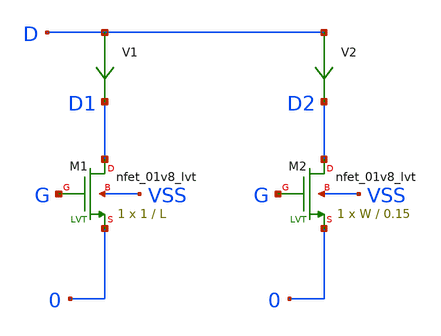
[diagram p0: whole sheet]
** sch_path: xyce/sky130A-xyce/libs.tech/xschem/sky130_tests/test_nmos_sizes.sch
* Copyright 2020 Stefan Frederik Schippers
* Licensed under the Apache License, Version 2.0 (the "License");
* you may not use this file except in compliance with the License.
* You may obtain a copy of the License at
* https://www.apache.org/licenses/LICENSE-2.0
* Unless required by applicable law or agreed to in writing, software
* distributed under the License is distributed on an "AS IS" BASIS,
* WITHOUT WARRANTIES OR CONDITIONS OF ANY KIND, either express or implied.
* See the License for the specific language governing permissions and
* limitations under the License.
**.subckt test_nmos_sizes
XM1 D1 G 0 VSS sky130_fd_pr__nfet_01v8_lvt L=L W=1 nf=1 ad='W * 0.29' as='W * 0.29' pd='2 * (W + 0.29)'
+ ps='2 * (W + 0.29)' nrd='0.29 / W' nrs='0.29 / W' sa=0 sb=0 sd=0 mult=1 m=1
XM2 D2 G 0 VSS sky130_fd_pr__nfet_01v8_lvt L=0.15 W=W nf=1 ad='W * 0.29' as='W * 0.29' pd='2 * (W + 0.29)'
+ ps='2 * (W + 0.29)' nrd='0.29 / W' nrs='0.29 / W' sa=0 sb=0 sd=0 mult=1 m=1
V2 D D2 0
.save i(v2)
V1 D D1 0
.save i(v1)
**** begin user architecture code

.include $::SKYWATER_MODELS/cells/nfet_01v8/sky130_fd_pr__nfet_01v8__tt.corner.spice
.include $::SKYWATER_MODELS/cells/nfet_01v8_lvt/sky130_fd_pr__nfet_01v8_lvt__tt.corner.spice
.include $::SKYWATER_MODELS/cells/pfet_01v8/sky130_fd_pr__pfet_01v8__tt.corner.spice
.include $::SKYWATER_MODELS/cells/nfet_03v3_nvt/sky130_fd_pr__nfet_03v3_nvt__tt.corner.spice
.include $::SKYWATER_MODELS/cells/nfet_05v0_nvt/sky130_fd_pr__nfet_05v0_nvt__tt.corner.spice
.include $::SKYWATER_MODELS/cells/esd_nfet_01v8/sky130_fd_pr__esd_nfet_01v8__tt.corner.spice
.include $::SKYWATER_MODELS/cells/pfet_01v8_lvt/sky130_fd_pr__pfet_01v8_lvt__tt.corner.spice
.include $::SKYWATER_MODELS/cells/pfet_01v8_hvt/sky130_fd_pr__pfet_01v8_hvt__tt.corner.spice
.include $::SKYWATER_MODELS/cells/esd_pfet_g5v0d10v5/sky130_fd_pr__esd_pfet_g5v0d10v5__tt.corner.spice
.include $::SKYWATER_MODELS/cells/pfet_g5v0d10v5/sky130_fd_pr__pfet_g5v0d10v5__tt.corner.spice
.include $::SKYWATER_MODELS/cells/pfet_g5v0d16v0/sky130_fd_pr__pfet_g5v0d16v0__tt.corner.spice
.include $::SKYWATER_MODELS/cells/nfet_g5v0d10v5/sky130_fd_pr__nfet_g5v0d10v5__tt.corner.spice
.include $::SKYWATER_MODELS/cells/nfet_g5v0d16v0/sky130_fd_pr__nfet_g5v0d16v0__tt_discrete.corner.spice
.include $::SKYWATER_MODELS/cells/esd_nfet_g5v0d10v5/sky130_fd_pr__esd_nfet_g5v0d10v5__tt.corner.spice
.include $::SKYWATER_MODELS/models/corners/tt/nonfet.spice
* Mismatch parameters
.include $::SKYWATER_MODELS/cells/nfet_01v8/sky130_fd_pr__nfet_01v8__mismatch.corner.spice
.include $::SKYWATER_MODELS/cells/pfet_01v8/sky130_fd_pr__pfet_01v8__mismatch.corner.spice
.include $::SKYWATER_MODELS/cells/nfet_01v8_lvt/sky130_fd_pr__nfet_01v8_lvt__mismatch.corner.spice
.include $::SKYWATER_MODELS/cells/pfet_01v8_lvt/sky130_fd_pr__pfet_01v8_lvt__mismatch.corner.spice
.include $::SKYWATER_MODELS/cells/pfet_01v8_hvt/sky130_fd_pr__pfet_01v8_hvt__mismatch.corner.spice
.include $::SKYWATER_MODELS/cells/nfet_g5v0d10v5/sky130_fd_pr__nfet_g5v0d10v5__mismatch.corner.spice
.include $::SKYWATER_MODELS/cells/pfet_g5v0d10v5/sky130_fd_pr__pfet_g5v0d10v5__mismatch.corner.spice
.include $::SKYWATER_MODELS/cells/nfet_05v0_nvt/sky130_fd_pr__nfet_05v0_nvt__mismatch.corner.spice
.include $::SKYWATER_MODELS/cells/nfet_03v3_nvt/sky130_fd_pr__nfet_03v3_nvt__mismatch.corner.spice
* Resistor$::SKYWATER_MODELS/Capacitor
.include $::SKYWATER_MODELS/models/r+c/res_typical__cap_typical.spice
.include $::SKYWATER_MODELS/models/r+c/res_typical__cap_typical__lin.spice
* Special cells
.include $::SKYWATER_MODELS/models/corners/tt/specialized_cells.spice
* All models
.include $::SKYWATER_MODELS/models/all.spice
* Corner
.include $::SKYWATER_MODELS/models/corners/tt/rf.spice

**** end user architecture code
**.ends
**** begin user architecture code

* .option SCALE=1e-6
.option method=gear seed=12
.param L=0.15
.param W=0.5

vd d 0 0
vg g 0 0
.control
dc vd 0 2 0.01 vg 0 2 0.2
alterparam L=0.18
alterparam W=1
reset
dc vd 0 2 0.01 vg 0 2 0.2
alterparam L=0.3
alterparam W=2
reset
dc vd 0 2 0.01 vg 0 2 0.2
alterparam L=0.5
alterparam W=3
reset
dc vd 0 2 0.01 vg 0 2 0.2

.endc





**** end user architecture code
.end
